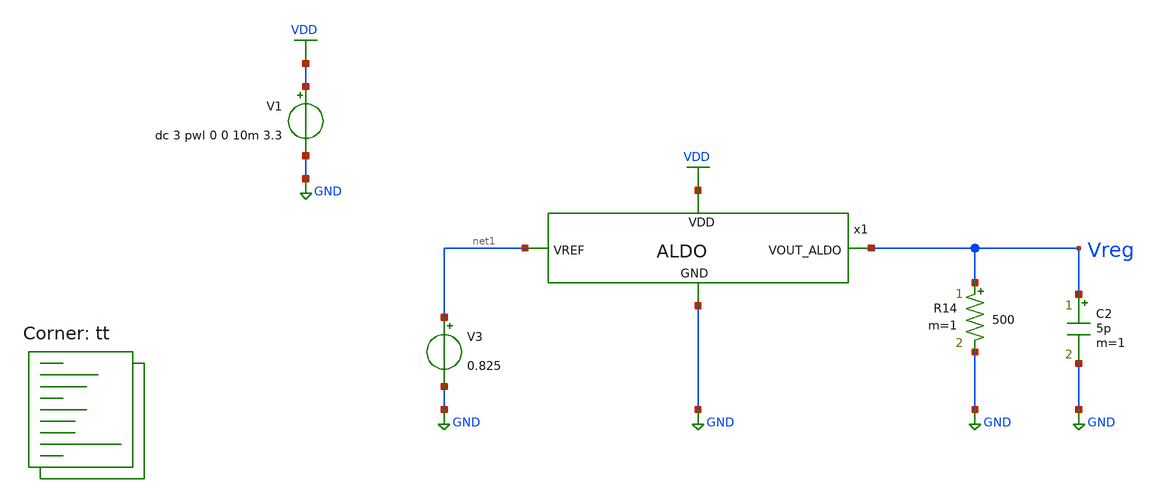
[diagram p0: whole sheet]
** sch_path: ALDO/Testbenches/ALDO_tb1.sch
**.subckt ALDO_tb1
x1 VDD Vreg net1 GND ALDO
V1 VDD GND dc 3 pwl 0 0 10m 3.3
V3 net1 GND 0.825
C2 Vreg GND 5p m=1
R14 Vreg GND 500 m=1
**** begin user architecture code


.option wnflag=1
.option savecurrents sparse $ ITL1=2000 ITL2=500 GMINSTEPS=100
.temp 27
.control
save all
op
write LDO1_stef.raw
set appendwrite
dc V1 0 3.3 10m
plot v(vreg)
write ALDO_tb1.raw
tran 10u 10m uic
write ALDO_tb1.raw
* plot v(vreg)
**quit 0
.endc


.lib $::SKYWATER_MODELS/sky130.lib.spice tt
**** end user architecture code
**.ends

* expanding   symbol:  /foss/designs/Sims/IITGN/ALDO/ALDO.sym # of pins=4
** sym_path: ALDO/Schematic/Testbenches/ALDO.sym
** sch_path: ALDO/Schematic/Testbenches/ALDO.sch
.subckt ALDO VDD VOUT_ALDO VREF GND
*.ipin VREF
*.ipin VDD
*.ipin GND
*.opin VOUT_ALDO
XM11 VOUT_ALDO vctrl VDD VDD sky130_fd_pr__pfet_g5v0d10v5 L=0.5 W=30.15 nf=1 ad='int((nf+1)/2) * W/nf * 0.29'
+ as='int((nf+2)/2) * W/nf * 0.29' pd='2*int((nf+1)/2) * (W/nf + 0.29)' ps='2*int((nf+2)/2) * (W/nf + 0.29)'
+ nrd='0.29 / W' nrs='0.29 / W' sa=0 sb=0 sd=0 mult=100 m=100
XM16 net1 net1 GND GND sky130_fd_pr__nfet_01v8 L=2 W=2.5 nf=1 ad='int((nf+1)/2) * W/nf * 0.29' as='int((nf+2)/2) * W/nf * 0.29'
+ pd='2*int((nf+1)/2) * (W/nf + 0.29)' ps='2*int((nf+2)/2) * (W/nf + 0.29)' nrd='0.29 / W' nrs='0.29 / W'
+ sa=0 sb=0 sd=0 mult=4 m=4
XM3 vctrl net3 VDD VDD sky130_fd_pr__pfet_g5v0d10v5 L=2 W=18 nf=1 ad='int((nf+1)/2) * W/nf * 0.29' as='int((nf+2)/2) * W/nf * 0.29'
+ pd='2*int((nf+1)/2) * (W/nf + 0.29)' ps='2*int((nf+2)/2) * (W/nf + 0.29)' nrd='0.29 / W' nrs='0.29 / W'
+ sa=0 sb=0 sd=0 mult=4 m=4
XM17 net3 net3 VDD VDD sky130_fd_pr__pfet_g5v0d10v5 L=2 W=18 nf=1 ad='int((nf+1)/2) * W/nf * 0.29' as='int((nf+2)/2) * W/nf * 0.29'
+ pd='2*int((nf+1)/2) * (W/nf + 0.29)' ps='2*int((nf+2)/2) * (W/nf + 0.29)' nrd='0.29 / W' nrs='0.29 / W'
+ sa=0 sb=0 sd=0 mult=4 m=4
XR47 VDD net6 GND sky130_fd_pr__res_xhigh_po_1p41 L=2.05 mult=1 m=1
XR5 net6 net7 GND sky130_fd_pr__res_xhigh_po_1p41 L=2.05 mult=1 m=1
XR6 net7 net8 GND sky130_fd_pr__res_xhigh_po_1p41 L=2.05 mult=1 m=1
XR7 net8 net9 GND sky130_fd_pr__res_xhigh_po_1p41 L=2.05 mult=1 m=1
XR8 net10 net1 GND sky130_fd_pr__res_xhigh_po_1p41 L=2.05 mult=1 m=1
XR9 net11 net10 GND sky130_fd_pr__res_xhigh_po_1p41 L=2.05 mult=1 m=1
XR10 net12 net11 GND sky130_fd_pr__res_xhigh_po_1p41 L=2.05 mult=1 m=1
XR11 net9 net12 GND sky130_fd_pr__res_xhigh_po_1p41 L=2.05 mult=1 m=1
XR27 VOUT_ALDO net13 GND sky130_fd_pr__res_xhigh_po_1p41 L=8.7 mult=1 m=1
XR28 net13 net14 GND sky130_fd_pr__res_xhigh_po_1p41 L=8.7 mult=1 m=1
XR29 net14 net15 GND sky130_fd_pr__res_xhigh_po_1p41 L=8.7 mult=1 m=1
XR30 net15 net16 GND sky130_fd_pr__res_xhigh_po_1p41 L=8.7 mult=1 m=1
XR31 net17 net18 GND sky130_fd_pr__res_xhigh_po_1p41 L=8.7 mult=1 m=1
XR32 net19 net17 GND sky130_fd_pr__res_xhigh_po_1p41 L=8.7 mult=1 m=1
XR33 net16 net19 GND sky130_fd_pr__res_xhigh_po_1p41 L=8.7 mult=1 m=1
XR34 net18 vfb GND sky130_fd_pr__res_xhigh_po_1p41 L=8.7 mult=1 m=1
XR35 net20 net21 GND sky130_fd_pr__res_xhigh_po_1p41 L=8.7 mult=1 m=1
XR36 net22 net20 GND sky130_fd_pr__res_xhigh_po_1p41 L=8.7 mult=1 m=1
XR37 net23 net22 GND sky130_fd_pr__res_xhigh_po_1p41 L=8.7 mult=1 m=1
XR38 net24 net23 GND sky130_fd_pr__res_xhigh_po_1p41 L=8.7 mult=1 m=1
XR39 net25 net24 GND sky130_fd_pr__res_xhigh_po_1p41 L=8.7 mult=1 m=1
XR40 net26 net25 GND sky130_fd_pr__res_xhigh_po_1p41 L=8.7 mult=1 m=1
XR41 vfb net26 GND sky130_fd_pr__res_xhigh_po_1p41 L=8.7 mult=1 m=1
XR42 net21 GND GND sky130_fd_pr__res_xhigh_po_1p41 L=8.7 mult=1 m=1
XC1 vctrl VOUT_ALDO sky130_fd_pr__cap_mim_m3_1 W=13.5 L=13.5 MF=8 m=8
XM6 net2 net1 GND GND sky130_fd_pr__nfet_01v8 L=2 W=2.5 nf=1 ad='int((nf+1)/2) * W/nf * 0.29' as='int((nf+2)/2) * W/nf * 0.29'
+ pd='2*int((nf+1)/2) * (W/nf + 0.29)' ps='2*int((nf+2)/2) * (W/nf + 0.29)' nrd='0.29 / W' nrs='0.29 / W'
+ sa=0 sb=0 sd=0 mult=4 m=4
XM7 net4 vfb net2 GND sky130_fd_pr__nfet_01v8_lvt L=1 W=5 nf=1 ad='int((nf+1)/2) * W/nf * 0.29' as='int((nf+2)/2) * W/nf * 0.29'
+ pd='2*int((nf+1)/2) * (W/nf + 0.29)' ps='2*int((nf+2)/2) * (W/nf + 0.29)' nrd='0.29 / W' nrs='0.29 / W'
+ sa=0 sb=0 sd=0 mult=4 m=4
XM4 net5 VREF net2 GND sky130_fd_pr__nfet_01v8_lvt L=1 W=5 nf=1 ad='int((nf+1)/2) * W/nf * 0.29' as='int((nf+2)/2) * W/nf * 0.29'
+ pd='2*int((nf+1)/2) * (W/nf + 0.29)' ps='2*int((nf+2)/2) * (W/nf + 0.29)' nrd='0.29 / W' nrs='0.29 / W'
+ sa=0 sb=0 sd=0 mult=4 m=4
XM1 net3 vfb net4 GND sky130_fd_pr__nfet_05v0_nvt L=0.9 W=1 nf=1 ad='int((nf+1)/2) * W/nf * 0.29' as='int((nf+2)/2) * W/nf * 0.29'
+ pd='2*int((nf+1)/2) * (W/nf + 0.29)' ps='2*int((nf+2)/2) * (W/nf + 0.29)' nrd='0.29 / W' nrs='0.29 / W'
+ sa=0 sb=0 sd=0 mult=8 m=8
XM2 vctrl VREF net5 GND sky130_fd_pr__nfet_05v0_nvt L=0.9 W=1 nf=1 ad='int((nf+1)/2) * W/nf * 0.29' as='int((nf+2)/2) * W/nf * 0.29'
+ pd='2*int((nf+1)/2) * (W/nf + 0.29)' ps='2*int((nf+2)/2) * (W/nf + 0.29)' nrd='0.29 / W' nrs='0.29 / W'
+ sa=0 sb=0 sd=0 mult=8 m=8
.ends

.GLOBAL GND
.GLOBAL VDD
.end
